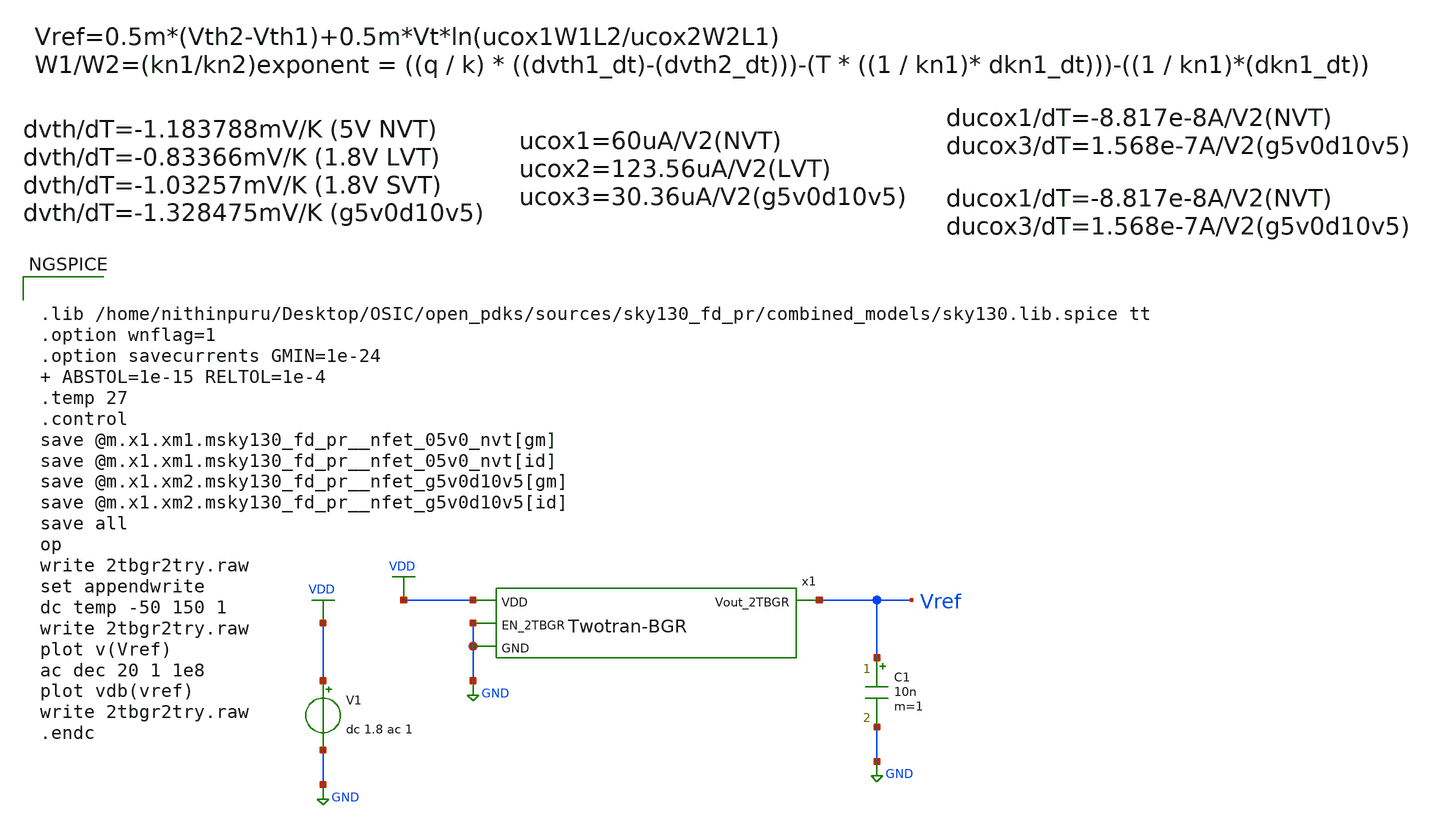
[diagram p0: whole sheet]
** sch_path: 2TBGR/Schematics/2tbgr2try.sch
**.subckt 2tbgr2try
V1 VDD GND dc 1.8 ac 1
x1 VDD GND Vref GND Twotran-BGR
C1 Vref GND 10n m=1
**** begin user architecture code


.lib /home/nithinpuru/Desktop/OSIC/open_pdks/sources/sky130_fd_pr/combined_models/sky130.lib.spice tt
.option wnflag=1
.option savecurrents GMIN=1e-24  ABSTOL=1e-15 RELTOL=1e-4
.temp 27
.control
save @m.x1.xm1.msky130_fd_pr__nfet_05v0_nvt[gm]
save @m.x1.xm1.msky130_fd_pr__nfet_05v0_nvt[id]
save @m.x1.xm2.msky130_fd_pr__nfet_g5v0d10v5[gm]
save @m.x1.xm2.msky130_fd_pr__nfet_g5v0d10v5[id]
save all
op
write 2tbgr2try.raw
set appendwrite
dc temp -50 150 1
write 2tbgr2try.raw
plot v(Vref)
ac dec 20 1 1e8
plot vdb(vref)
write 2tbgr2try.raw
.endc


**** end user architecture code
**.ends

* expanding   symbol:  Sims/IITGN/2TBGR/Twotran-BGR.sym # of pins=4
** sym_path: 2TBGR/Schematics/Twotran-BGR.sym
** sch_path: 2TBGR/Schematics/Twotran-BGR.sch
.subckt Twotran-BGR VDD EN_2TBGR Vout_2TBGR GND
*.ipin GND
*.ipin VDD
*.opin Vout_2TBGR
*.ipin EN_2TBGR
XM3 VDD GND Vo2tbgr GND sky130_fd_pr__nfet_05v0_nvt L=20 W=17 nf=1 ad='int((nf+1)/2) * W/nf * 0.29' as='int((nf+2)/2) * W/nf * 0.29'
+ pd='2*int((nf+1)/2) * (W/nf + 0.29)' ps='2*int((nf+2)/2) * (W/nf + 0.29)' nrd='0.29 / W' nrs='0.29 / W'
+ sa=0 sb=0 sd=0 mult=1 m=1
XM1 Vo2tbgr Vo2tbgr GND GND sky130_fd_pr__nfet_g5v0d10v5 L=20 W=1 nf=1 ad='int((nf+1)/2) * W/nf * 0.29'
+ as='int((nf+2)/2) * W/nf * 0.29' pd='2*int((nf+1)/2) * (W/nf + 0.29)' ps='2*int((nf+2)/2) * (W/nf + 0.29)'
+ nrd='0.29 / W' nrs='0.29 / W' sa=0 sb=0 sd=0 mult=1 m=1
XM9 net2 net2 GND GND sky130_fd_pr__nfet_g5v0d10v5 L=2 W=4 nf=1 ad='int((nf+1)/2) * W/nf * 0.29' as='int((nf+2)/2) * W/nf * 0.29'
+ pd='2*int((nf+1)/2) * (W/nf + 0.29)' ps='2*int((nf+2)/2) * (W/nf + 0.29)' nrd='0.29 / W' nrs='0.29 / W'
+ sa=0 sb=0 sd=0 mult=1 m=1
XM10 net2 Vout_2TBGR net3 VDD sky130_fd_pr__pfet_g5v0d10v5 L=1.5 W=3 nf=1 ad='int((nf+1)/2) * W/nf * 0.29'
+ as='int((nf+2)/2) * W/nf * 0.29' pd='2*int((nf+1)/2) * (W/nf + 0.29)' ps='2*int((nf+2)/2) * (W/nf + 0.29)'
+ nrd='0.29 / W' nrs='0.29 / W' sa=0 sb=0 sd=0 mult=1 m=1
XM11 net1 Vo2tbgr net3 VDD sky130_fd_pr__pfet_g5v0d10v5 L=1.5 W=3 nf=1 ad='int((nf+1)/2) * W/nf * 0.29'
+ as='int((nf+2)/2) * W/nf * 0.29' pd='2*int((nf+1)/2) * (W/nf + 0.29)' ps='2*int((nf+2)/2) * (W/nf + 0.29)'
+ nrd='0.29 / W' nrs='0.29 / W' sa=0 sb=0 sd=0 mult=1 m=1
XM12 net1 net2 GND GND sky130_fd_pr__nfet_g5v0d10v5 L=2 W=4 nf=1 ad='int((nf+1)/2) * W/nf * 0.29' as='int((nf+2)/2) * W/nf * 0.29'
+ pd='2*int((nf+1)/2) * (W/nf + 0.29)' ps='2*int((nf+2)/2) * (W/nf + 0.29)' nrd='0.29 / W' nrs='0.29 / W'
+ sa=0 sb=0 sd=0 mult=1 m=1
XM13 net3 net4 VDD VDD sky130_fd_pr__pfet_g5v0d10v5 L=2 W=4 nf=1 ad='int((nf+1)/2) * W/nf * 0.29' as='int((nf+2)/2) * W/nf * 0.29'
+ pd='2*int((nf+1)/2) * (W/nf + 0.29)' ps='2*int((nf+2)/2) * (W/nf + 0.29)' nrd='0.29 / W' nrs='0.29 / W'
+ sa=0 sb=0 sd=0 mult=4 m=4
XM14 net4 net4 VDD VDD sky130_fd_pr__pfet_g5v0d10v5 L=2 W=4 nf=1 ad='int((nf+1)/2) * W/nf * 0.29' as='int((nf+2)/2) * W/nf * 0.29'
+ pd='2*int((nf+1)/2) * (W/nf + 0.29)' ps='2*int((nf+2)/2) * (W/nf + 0.29)' nrd='0.29 / W' nrs='0.29 / W'
+ sa=0 sb=0 sd=0 mult=4 m=4
XM15 Vout_2TBGR net4 VDD VDD sky130_fd_pr__pfet_g5v0d10v5 L=2 W=4 nf=1 ad='int((nf+1)/2) * W/nf * 0.29'
+ as='int((nf+2)/2) * W/nf * 0.29' pd='2*int((nf+1)/2) * (W/nf + 0.29)' ps='2*int((nf+2)/2) * (W/nf + 0.29)'
+ nrd='0.29 / W' nrs='0.29 / W' sa=0 sb=0 sd=0 mult=6 m=6
XM16 Vout_2TBGR net1 GND GND sky130_fd_pr__nfet_g5v0d10v5 L=1 W=5.5 nf=1 ad='int((nf+1)/2) * W/nf * 0.29'
+ as='int((nf+2)/2) * W/nf * 0.29' pd='2*int((nf+1)/2) * (W/nf + 0.29)' ps='2*int((nf+2)/2) * (W/nf + 0.29)'
+ nrd='0.29 / W' nrs='0.29 / W' sa=0 sb=0 sd=0 mult=4 m=4
XR5 net6 net5 GND sky130_fd_pr__res_xhigh_po_1p41 L=4.5 mult=1 m=1
XR6 net7 net6 GND sky130_fd_pr__res_xhigh_po_1p41 L=4.5 mult=1 m=1
XR7 net8 net7 GND sky130_fd_pr__res_xhigh_po_1p41 L=4.5 mult=1 m=1
XR8 net9 net8 GND sky130_fd_pr__res_xhigh_po_1p41 L=4.5 mult=1 m=1
XR9 net10 net9 GND sky130_fd_pr__res_xhigh_po_1p41 L=4.5 mult=1 m=1
XR10 net11 net10 GND sky130_fd_pr__res_xhigh_po_1p41 L=4.5 mult=1 m=1
XR11 GND net11 GND sky130_fd_pr__res_xhigh_po_1p41 L=4.5 mult=1 m=1
XM2 VDD VDD VDD VDD sky130_fd_pr__pfet_g5v0d10v5 L=1.5 W=3 nf=1 ad='int((nf+1)/2) * W/nf * 0.29' as='int((nf+2)/2) * W/nf * 0.29'
+ pd='2*int((nf+1)/2) * (W/nf + 0.29)' ps='2*int((nf+2)/2) * (W/nf + 0.29)' nrd='0.29 / W' nrs='0.29 / W'
+ sa=0 sb=0 sd=0 mult=6 m=6
XM4 VDD VDD VDD VDD sky130_fd_pr__pfet_g5v0d10v5 L=2 W=4 nf=1 ad='int((nf+1)/2) * W/nf * 0.29' as='int((nf+2)/2) * W/nf * 0.29'
+ pd='2*int((nf+1)/2) * (W/nf + 0.29)' ps='2*int((nf+2)/2) * (W/nf + 0.29)' nrd='0.29 / W' nrs='0.29 / W'
+ sa=0 sb=0 sd=0 mult=2 m=2
XM5 GND GND GND GND sky130_fd_pr__nfet_g5v0d10v5 L=2 W=4 nf=1 ad='int((nf+1)/2) * W/nf * 0.29' as='int((nf+2)/2) * W/nf * 0.29'
+ pd='2*int((nf+1)/2) * (W/nf + 0.29)' ps='2*int((nf+2)/2) * (W/nf + 0.29)' nrd='0.29 / W' nrs='0.29 / W'
+ sa=0 sb=0 sd=0 mult=6 m=6
XM6 GND GND GND GND sky130_fd_pr__nfet_g5v0d10v5 L=1 W=5.5 nf=1 ad='int((nf+1)/2) * W/nf * 0.29' as='int((nf+2)/2) * W/nf * 0.29'
+ pd='2*int((nf+1)/2) * (W/nf + 0.29)' ps='2*int((nf+2)/2) * (W/nf + 0.29)' nrd='0.29 / W' nrs='0.29 / W'
+ sa=0 sb=0 sd=0 mult=4 m=4
XM7 net4 EN_2TBGR net5 GND sky130_fd_pr__nfet_g5v0d10v5 L=0.5 W=8 nf=1 ad='int((nf+1)/2) * W/nf * 0.29'
+ as='int((nf+2)/2) * W/nf * 0.29' pd='2*int((nf+1)/2) * (W/nf + 0.29)' ps='2*int((nf+2)/2) * (W/nf + 0.29)'
+ nrd='0.29 / W' nrs='0.29 / W' sa=0 sb=0 sd=0 mult=10 m=10
.ends

.GLOBAL GND
.GLOBAL VDD
.end
